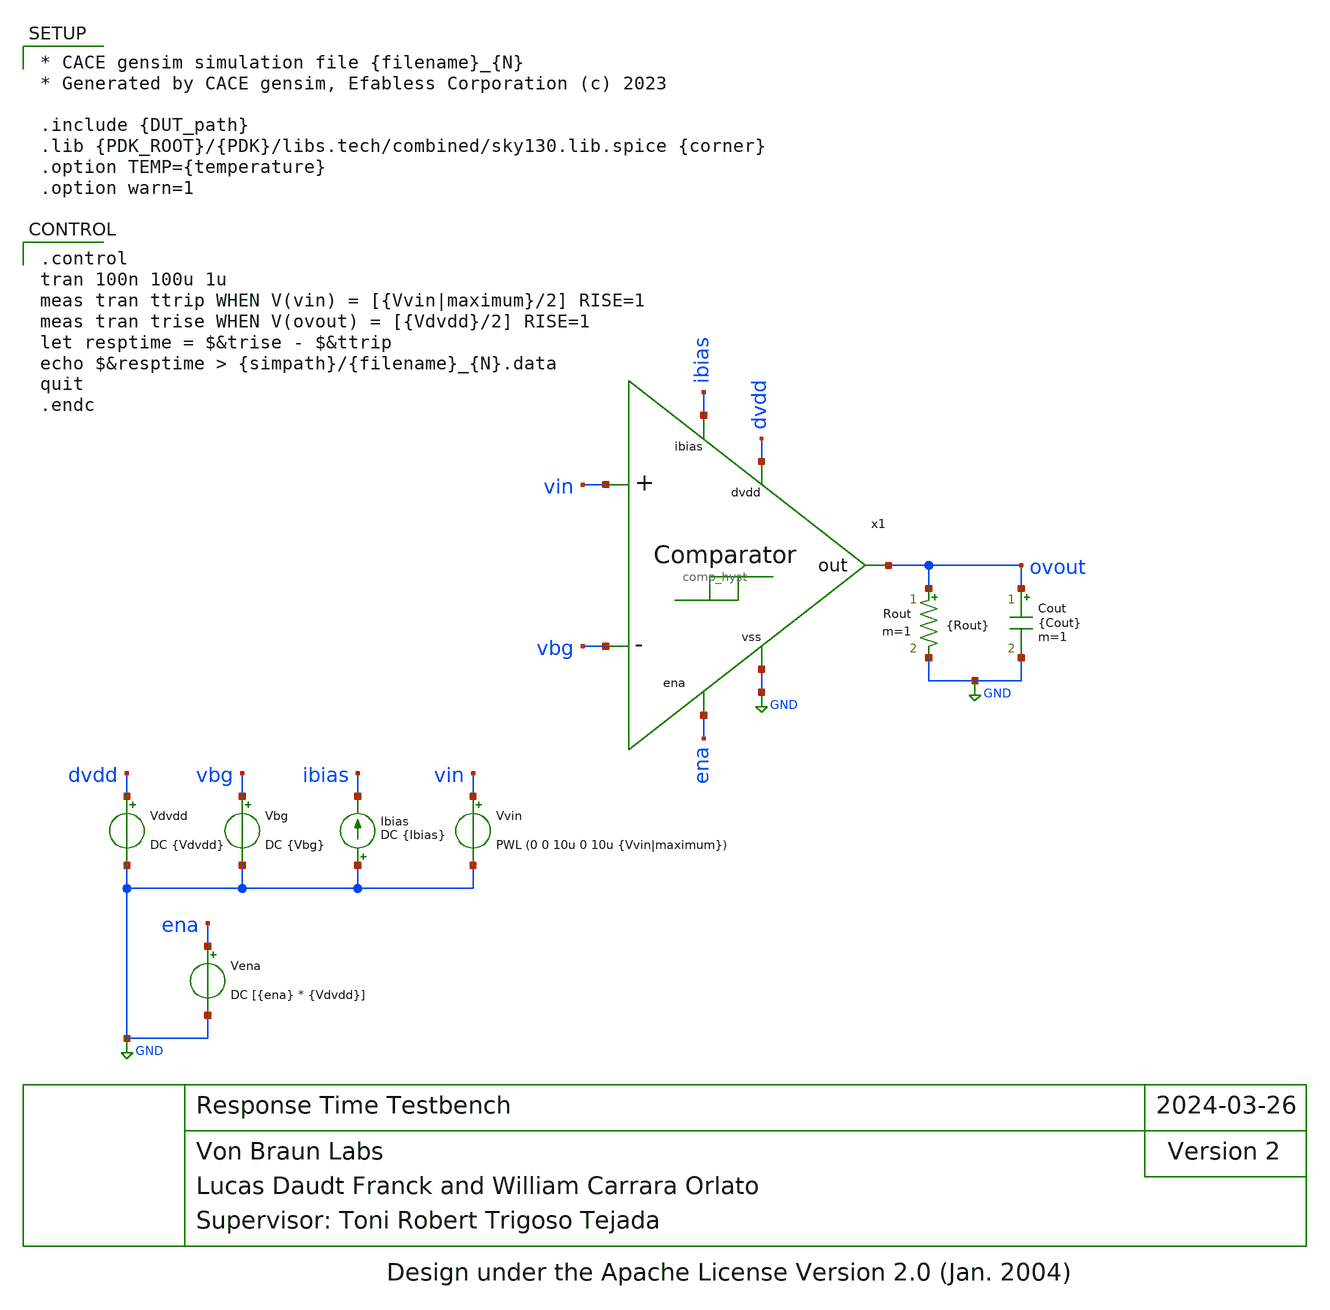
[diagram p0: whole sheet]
** sch_path: blocks/comp_hyst/cace/tb_resptime.sch
* Design under the Apache License Version 2.0 (Jan. 2004)
**.subckt tb_resptime
Vvin vin GND PWL (0 0 10u 0 10u {Vvin|maximum})
Vdvdd dvdd GND DC {Vdvdd}
Vbg vbg GND DC {Vbg}
Ibias GND ibias DC {Ibias}
Vena ena GND DC [{ena} * {Vdvdd}]
Cout ovout GND {Cout} m=1
Rout ovout GND {Rout} m=1
x1 dvdd ovout vbg vin ena ibias GND comp_hyst
**** begin user architecture code

* CACE gensim simulation file {filename}_{N}
* Generated by CACE gensim, Efabless Corporation (c) 2023

.include {DUT_path}
.lib {PDK_ROOT}/{PDK}/libs.tech/combined/sky130.lib.spice {corner}
.option TEMP={temperature}
.option warn=1



.control
tran 100n 100u 1u
meas tran ttrip WHEN V(vin) = [{Vvin|maximum}/2] RISE=1
meas tran trise WHEN V(ovout) = [{Vdvdd}/2] RISE=1
let resptime = $&trise - $&ttrip
echo $&resptime > {simpath}/{filename}_{N}.data
quit
.endc


**** end user architecture code
**.ends
.GLOBAL GND
.end
